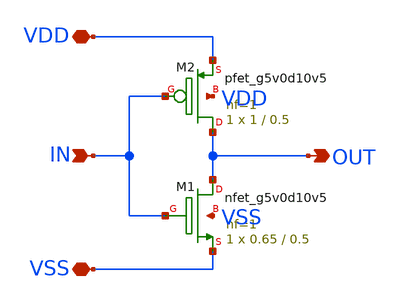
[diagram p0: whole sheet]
** sch_path: xschem/inverter.sch
**.subckt inverter VSS VDD IN OUT
*.iopin VSS
*.iopin VDD
*.ipin IN
*.opin OUT
XM1 OUT IN VSS VSS sky130_fd_pr__nfet_g5v0d10v5 L=0.5 W=0.65 nf=1 ad='int((1 + 1)/2) * 0.65 / 1 * 0.29'
+ as='int((1 + 2)/2) * 0.65 / 1 * 0.29' pd='2*int((1 + 1)/2) * (0.65 / 1 + 0.29)' ps='2*int((1 + 2)/2) * (0.65 / 1 + 0.29)'
+ nrd='0.29 / 0.65 ' nrs='0.29 / 0.65 ' sa=0 sb=0 sd=0 mult=1 m=1
XM2 OUT IN VDD VDD sky130_fd_pr__pfet_g5v0d10v5 L=0.5 W=1 nf=1 ad='int((1 + 1)/2) * 1 / 1 * 0.29' as='int((1 + 2)/2) * 1 / 1 * 0.29'
+ pd='2*int((1 + 1)/2) * (1 / 1 + 0.29)' ps='2*int((1 + 2)/2) * (1 / 1 + 0.29)' nrd='0.29 / 1 ' nrs='0.29 / 1 '
+ sa=0 sb=0 sd=0 mult=1 m=1
**.ends
.end
